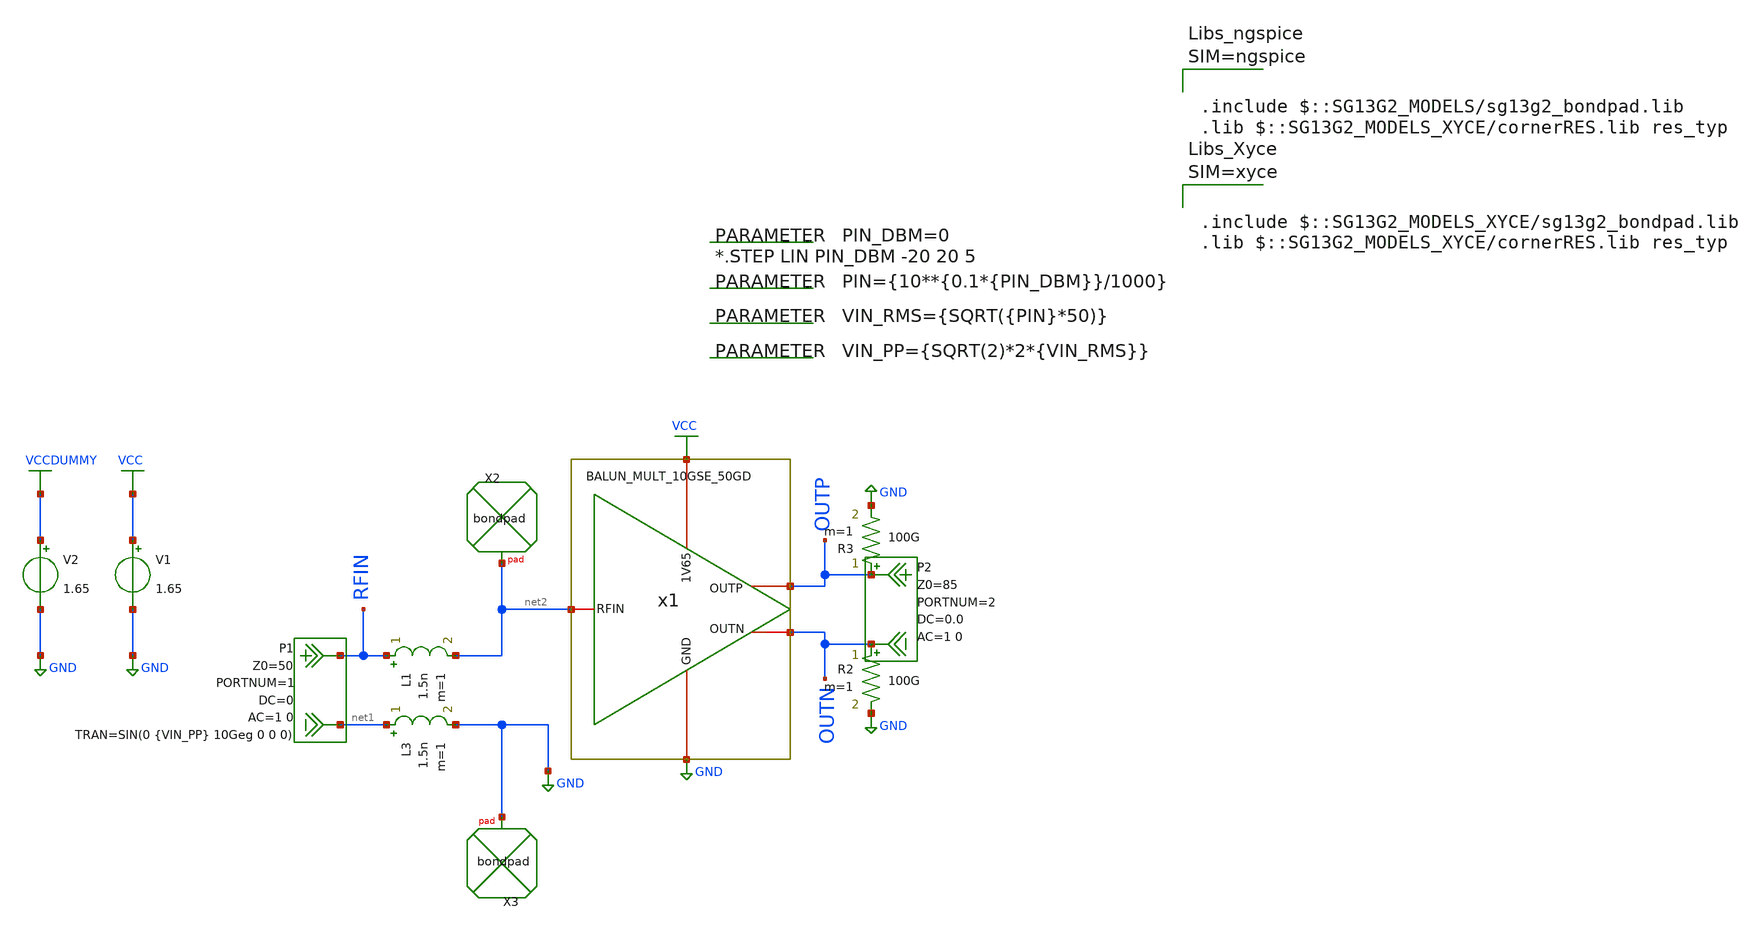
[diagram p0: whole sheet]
** sch_path: mWATTBAT/design_data/xschem/BALUN_MULT_10GSE_50GD_TB.sch
**.subckt BALUN_MULT_10GSE_50GD_TB
L1 RFIN net2 1.5n m=1
L3 net1 GND 1.5n m=1
.param PIN_DBM=0
*.STEP LIN PIN_DBM -20 20 5
.param PIN={10**{0.1*{PIN_DBM}}/1000}
.param VIN_RMS={SQRT({PIN}*50)}
.param VIN_PP={SQRT(2)*2*{VIN_RMS}}
V1 VCC GND 1.65
P2 OUTP OUTN 0.0 port=2 Z0=85 AC 1 0
XX2 net2 bondpad size=80u shape=0 padtype=0
XX3 GND bondpad size=80u shape=0 padtype=0
R2 OUTN GND 100G m=1
R3 OUTP GND 100G m=1
V2 VCCDUMMY GND 1.65
P1 RFIN net1 0 port=1 Z0=50 AC 1 0 SIN(0 {VIN_PP} 10Geg 0 0 0)
x1 OUTP OUTN VCC net2 GND BALUN_MULT_10GSE_50GD
**** begin user architecture code


.PREPROCESS REPLACEGROUND TRUE
.TRAN 10p 20n
*.TRAN 10p 200n
.MEAS TRAN ICC EQN {-1*I(V1)}
.MEAS TRAN ICC_RMS RMS I(V1)
.MEAS TRAN OUTD EQN V(OUTP,OUTN)
.PRINT TRAN FORMAT=RAW FILE=BALUN_MULT_10GSE_50GD_TBTRAN.raw V(*) I(*) ICC ICC_RMS OUTD
.FOUR 10G V(OUTP,OUTN)








.include $::SG13G2_MODELS/sg13g2_bondpad.lib
.lib $::SG13G2_MODELS_XYCE/cornerRES.lib res_typ



**** end user architecture code
**.ends
.GLOBAL VCC
.GLOBAL GND
.GLOBAL VCCDUMMY
.end
